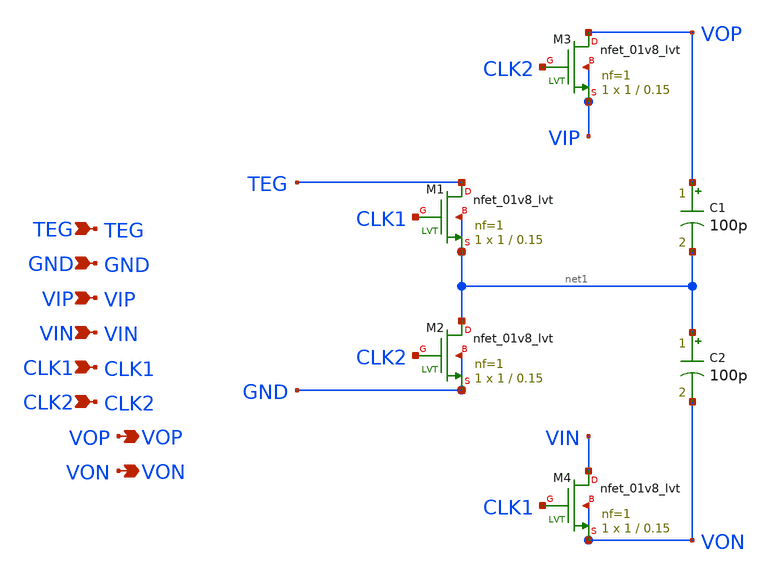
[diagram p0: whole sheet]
** sch_path: design/LELO_SC_MODULE.sch
**.subckt LELO_SC_MODULE TEG VOP GND VIP VIN CLK1 CLK2 VON
*.ipin TEG
*.opin VOP
*.ipin GND
*.ipin VIP
*.ipin VIN
*.ipin CLK1
*.ipin CLK2
*.opin VON
C1 VOP net1 100p m=1
C2 net1 VON 100p m=1
XM1 TEG CLK1 net1 net1 sky130_fd_pr__nfet_01v8_lvt L=0.15 W=1 nf=1 ad='int((1 + 1)/2) * 1 / 1 * 0.29'
+ as='int((1 + 2)/2) * 1 / 1 * 0.29' pd='2*int((1 + 1)/2) * (1 / 1 + 0.29)' ps='2*int((1 + 2)/2) * (1 / 1 + 0.29)'
+ nrd='0.29 / 1 ' nrs='0.29 / 1 ' sa=0 sb=0 sd=0 mult=1 m=1
XM2 net1 CLK2 GND GND sky130_fd_pr__nfet_01v8_lvt L=0.15 W=1 nf=1 ad='int((1 + 1)/2) * 1 / 1 * 0.29'
+ as='int((1 + 2)/2) * 1 / 1 * 0.29' pd='2*int((1 + 1)/2) * (1 / 1 + 0.29)' ps='2*int((1 + 2)/2) * (1 / 1 + 0.29)'
+ nrd='0.29 / 1 ' nrs='0.29 / 1 ' sa=0 sb=0 sd=0 mult=1 m=1
XM3 VOP CLK2 VIP VIP sky130_fd_pr__nfet_01v8_lvt L=0.15 W=1 nf=1 ad='int((1 + 1)/2) * 1 / 1 * 0.29' as='int((1 + 2)/2) * 1 / 1 * 0.29'
+ pd='2*int((1 + 1)/2) * (1 / 1 + 0.29)' ps='2*int((1 + 2)/2) * (1 / 1 + 0.29)' nrd='0.29 / 1 ' nrs='0.29 / 1 '
+ sa=0 sb=0 sd=0 mult=1 m=1
XM4 VIN CLK1 VON VON sky130_fd_pr__nfet_01v8_lvt L=0.15 W=1 nf=1 ad='int((1 + 1)/2) * 1 / 1 * 0.29' as='int((1 + 2)/2) * 1 / 1 * 0.29'
+ pd='2*int((1 + 1)/2) * (1 / 1 + 0.29)' ps='2*int((1 + 2)/2) * (1 / 1 + 0.29)' nrd='0.29 / 1 ' nrs='0.29 / 1 '
+ sa=0 sb=0 sd=0 mult=1 m=1
**.ends
.end
